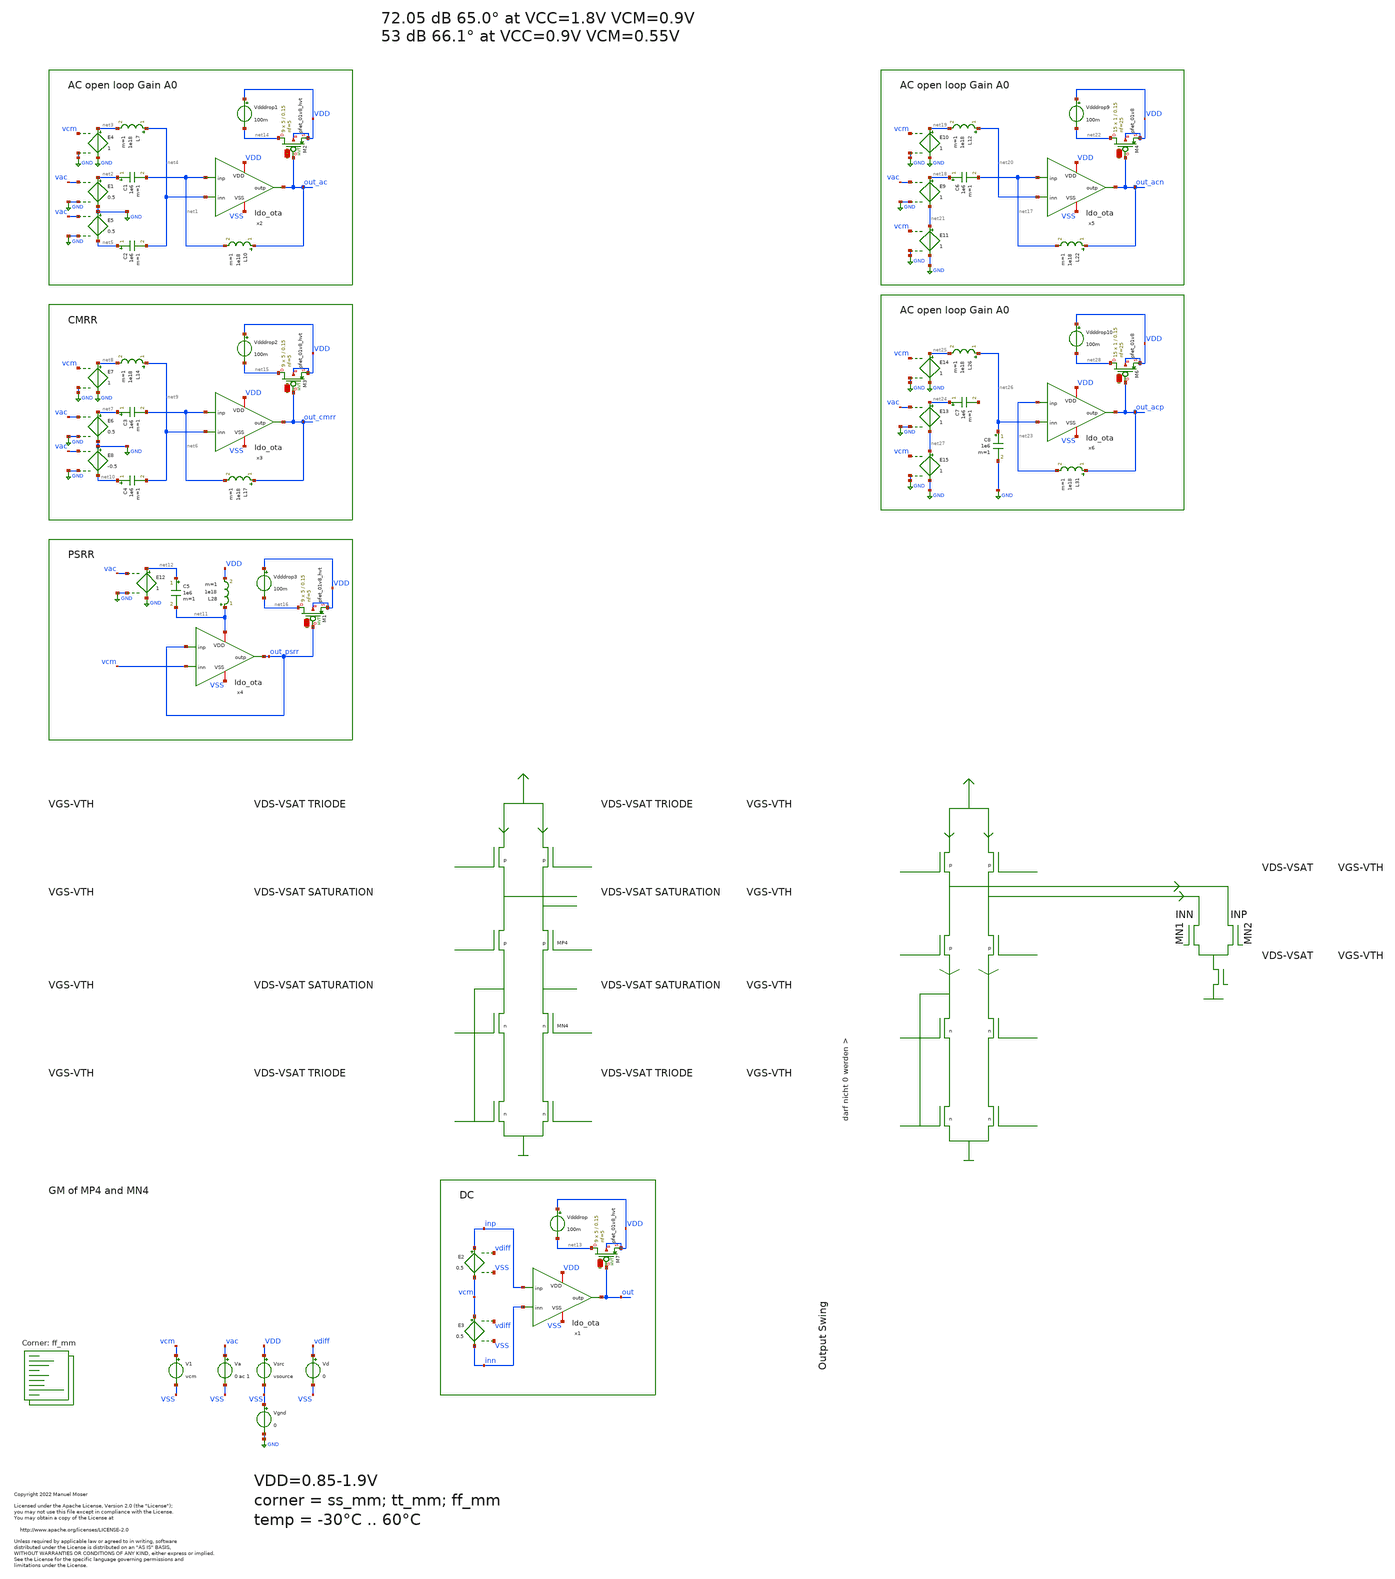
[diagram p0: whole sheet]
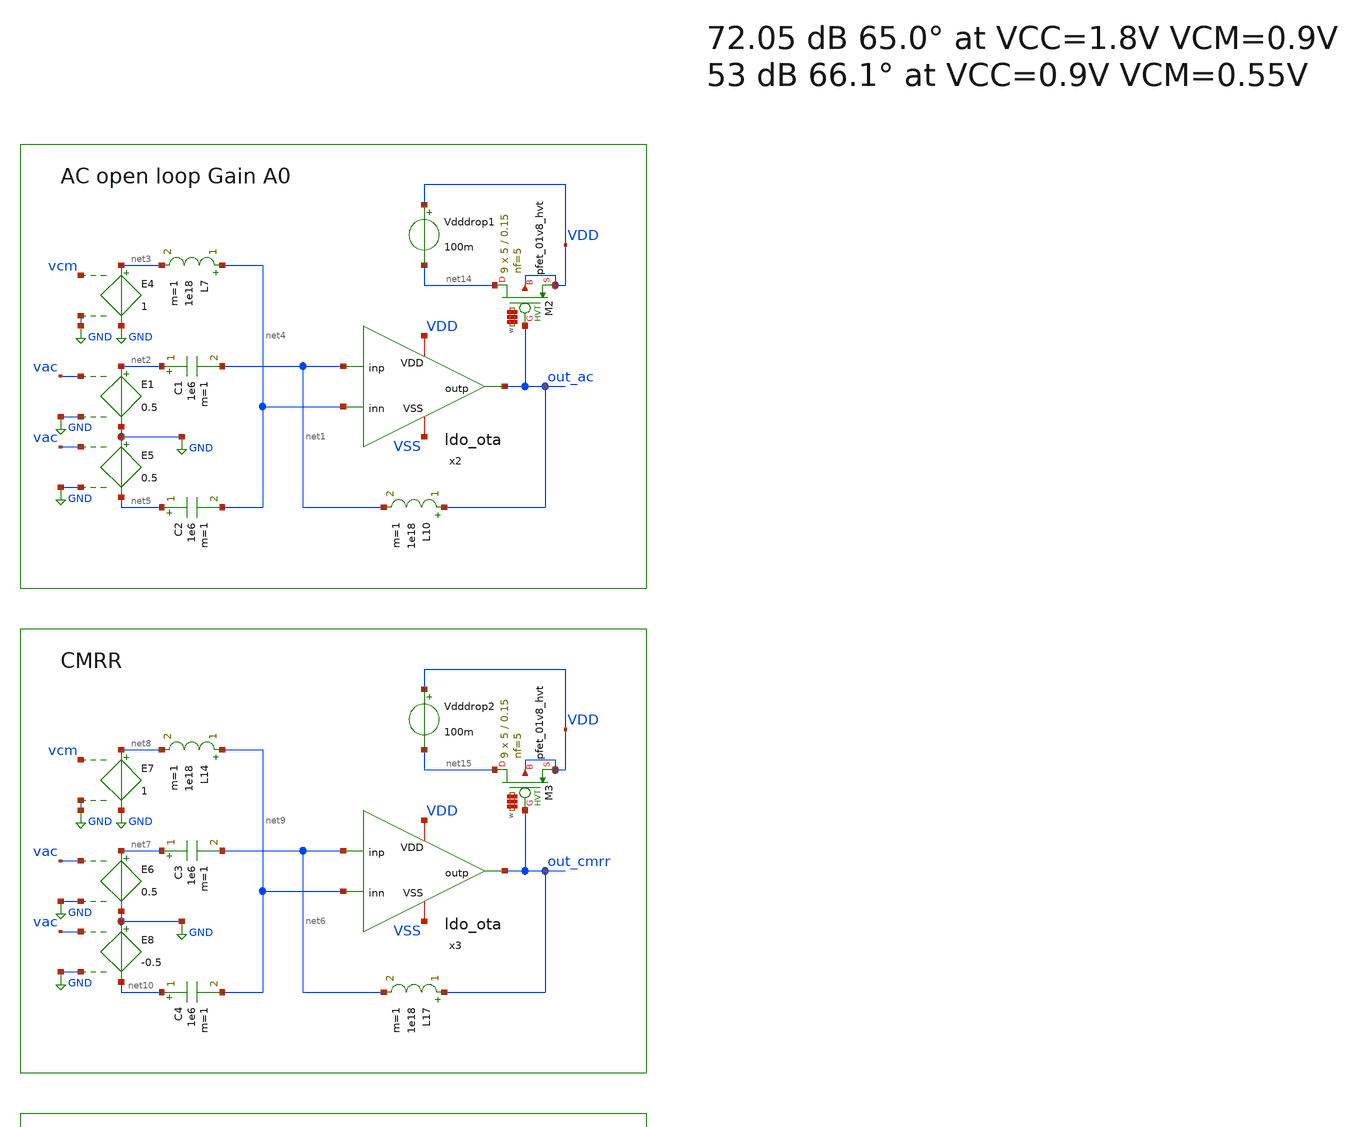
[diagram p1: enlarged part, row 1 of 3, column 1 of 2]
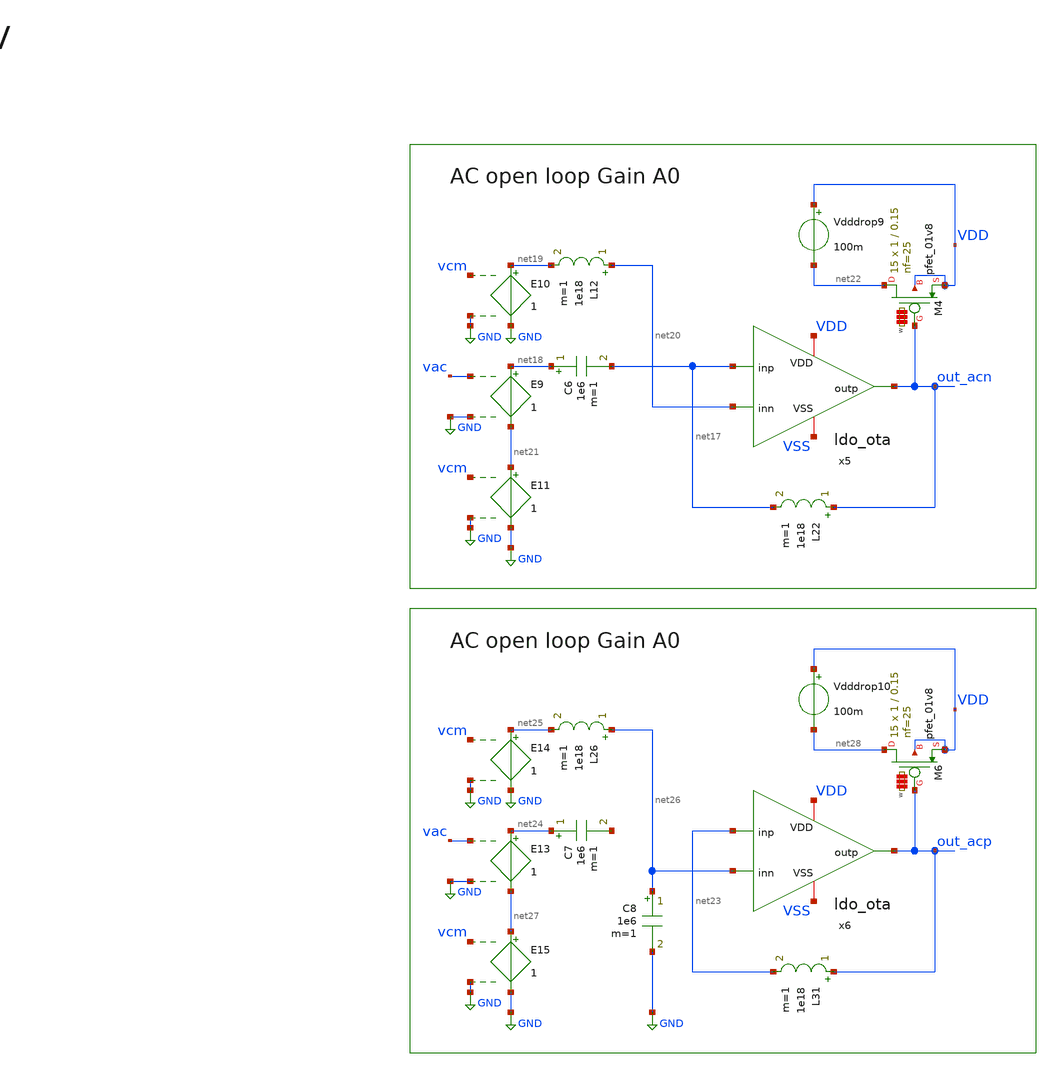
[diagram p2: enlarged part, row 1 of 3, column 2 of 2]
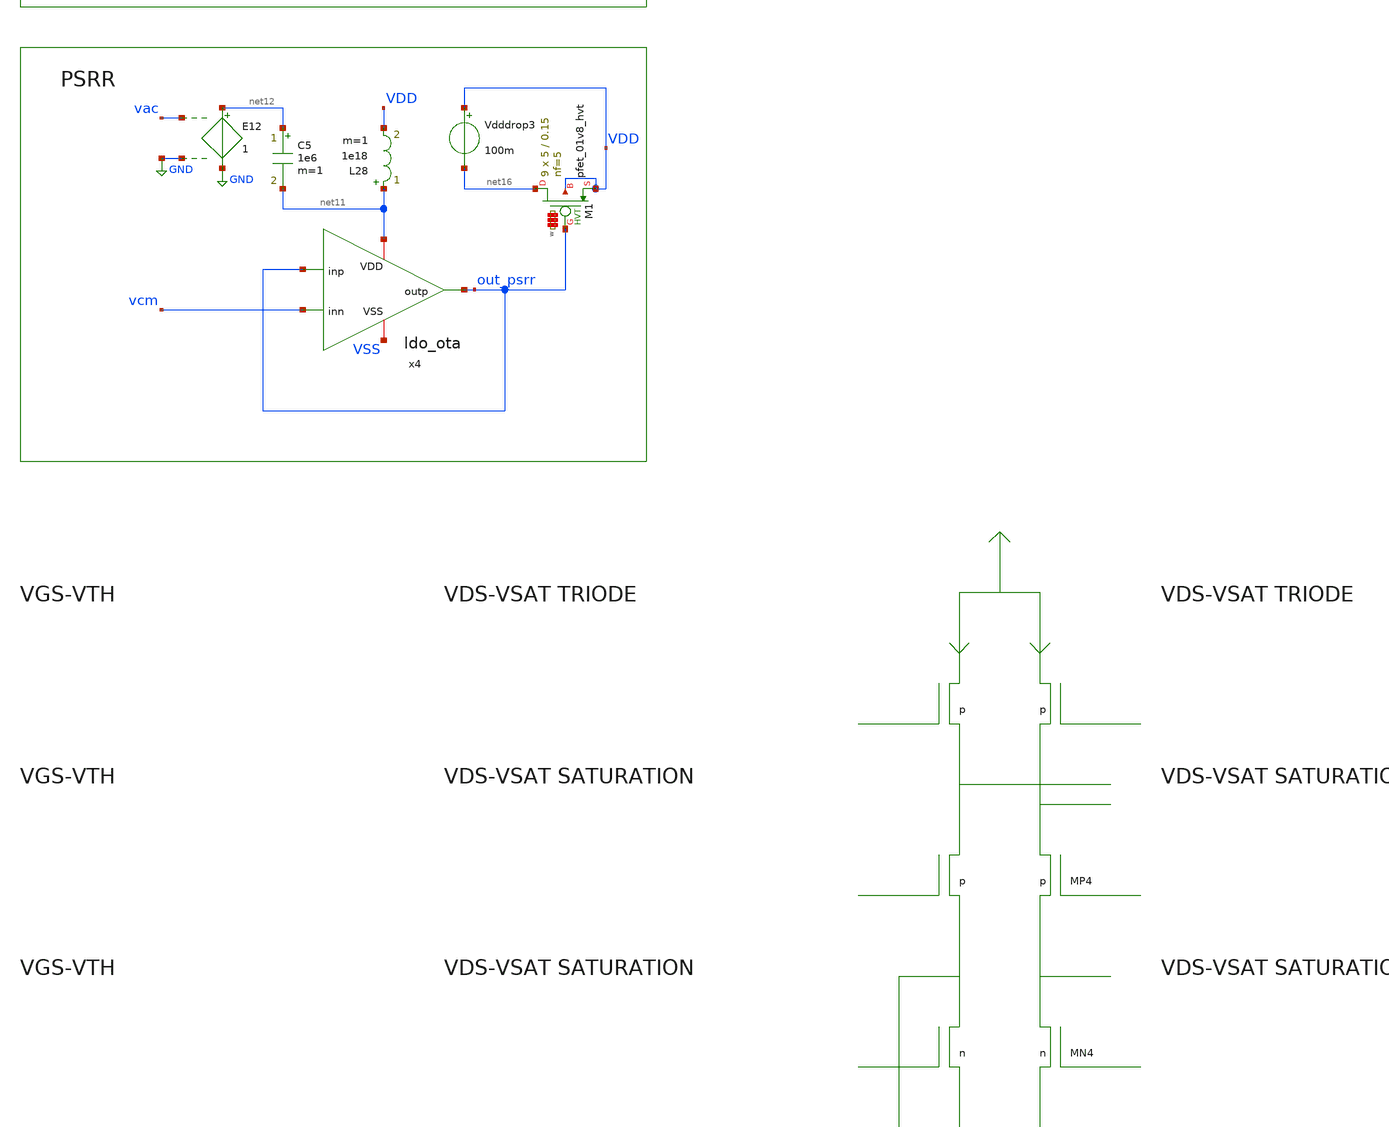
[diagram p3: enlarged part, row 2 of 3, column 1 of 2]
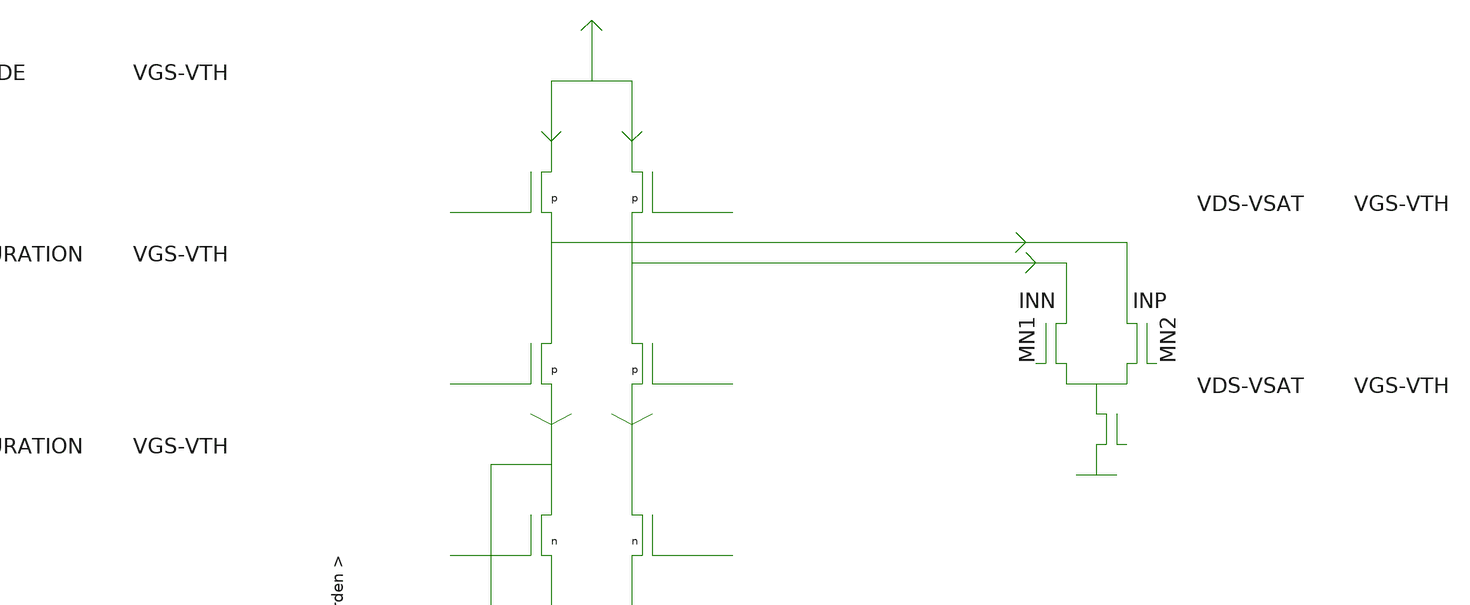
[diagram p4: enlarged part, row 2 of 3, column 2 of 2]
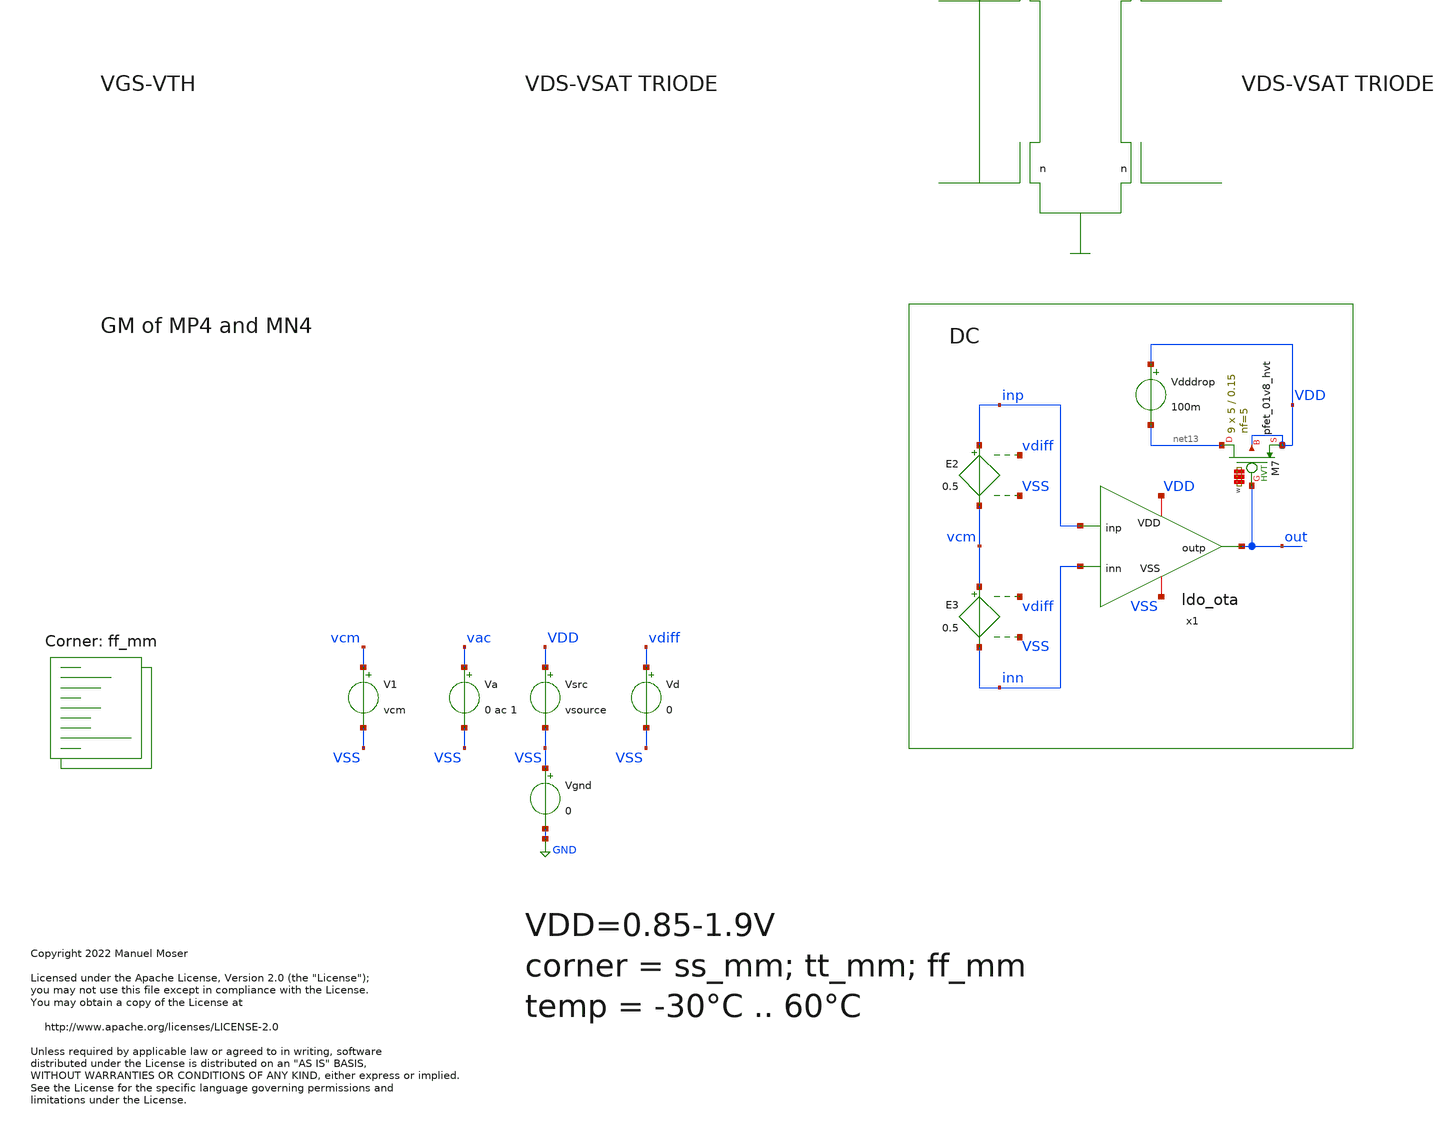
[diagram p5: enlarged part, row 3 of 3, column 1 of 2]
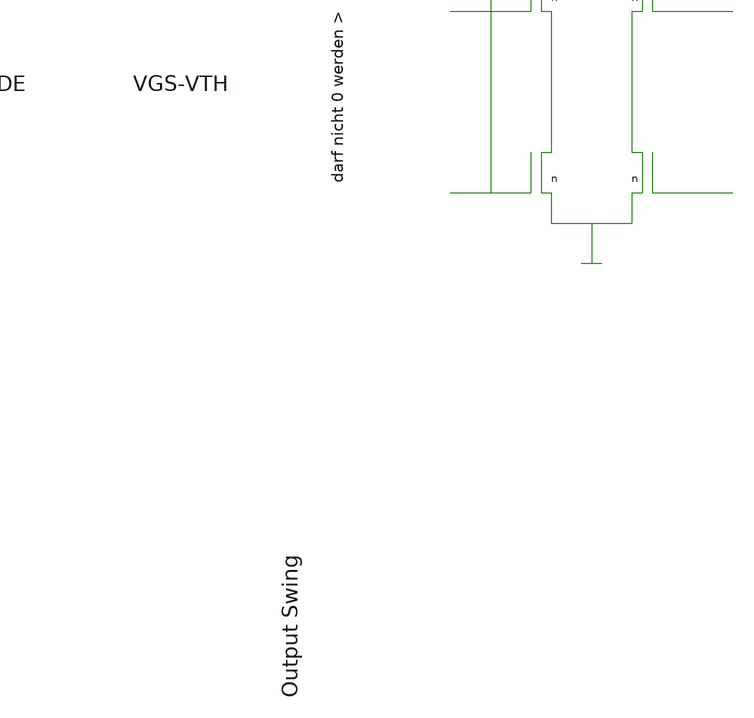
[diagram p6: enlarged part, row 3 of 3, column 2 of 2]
** sch_path: xschem/ldo_ota_tb.sch
* Copyright 2022 Manuel Moser
* Licensed under the Apache License, Version 2.0 (the "License");
**.subckt ldo_ota_tb
V1 vcm VSS vcm
Vd vdiff VSS 0
Vsrc VDD VSS vsource
E2 inp vcm vdiff VSS 0.5
E3 vcm inn vdiff VSS 0.5
Vgnd VSS GND 0
x2 VDD net1 out_ac net4 VSS ldo_ota
Va vac VSS 0 ac 1
E1 net2 GND vac GND 0.5
C1 net2 net1 1e6 m=1
L7 net4 net3 1e18 m=1
E4 net3 GND vcm GND 1
L10 out_ac net1 1e18 m=1
E5 GND net5 vac GND 0.5
C2 net5 net4 1e6 m=1
x3 VDD net6 out_cmrr net9 VSS ldo_ota
E6 net7 GND vac GND 0.5
C3 net7 net6 1e6 m=1
L14 net9 net8 1e18 m=1
E7 net8 GND vcm GND 1
L17 out_cmrr net6 1e18 m=1
E8 GND net10 vac GND -0.5
C4 net10 net9 1e6 m=1
x4 net11 out_psrr out_psrr vcm VSS ldo_ota
C5 net12 net11 1e6 m=1
L28 net11 VDD 1e18 m=1
E12 net12 GND vac GND 1
Vdddrop VDD net13 100m
Vdddrop1 VDD net14 100m
Vdddrop2 VDD net15 100m
Vdddrop3 VDD net16 100m
x1 VDD inp out inn VSS ldo_ota
x5 VDD net17 out_acn net20 VSS ldo_ota
E9 net18 net21 vac GND 1
C6 net18 net17 1e6 m=1
L12 net20 net19 1e18 m=1
E10 net19 GND vcm GND 1
L22 out_acn net17 1e18 m=1
Vdddrop9 VDD net22 100m
XM4 net22 out_acn VDD VDD sky130_fd_pr__pfet_01v8 L=0.15 W='1 * 25 ' nf=25 ad='int((nf+1)/2) * W / nf * 0.29'
+ as='int((nf+2)/2) * W / nf * 0.29' pd='2*int((nf+1)/2) * (W / nf + 0.29)' ps='2*int((nf+2)/2) * (W / nf + 0.29)'
+ nrd='0.29 / W ' nrs='0.29 / W ' sa=0 sb=0 sd=0 mult=15 m=15
E11 net21 GND vcm GND 1
E13 net24 net27 vac GND 1
C7 net24 net29 1e6 m=1
L26 net26 net25 1e18 m=1
E14 net25 GND vcm GND 1
L31 out_acp net23 1e18 m=1
Vdddrop10 VDD net28 100m
XM6 net28 out_acp VDD VDD sky130_fd_pr__pfet_01v8 L=0.15 W='1 * 25 ' nf=25 ad='int((nf+1)/2) * W / nf * 0.29'
+ as='int((nf+2)/2) * W / nf * 0.29' pd='2*int((nf+1)/2) * (W / nf + 0.29)' ps='2*int((nf+2)/2) * (W / nf + 0.29)'
+ nrd='0.29 / W ' nrs='0.29 / W ' sa=0 sb=0 sd=0 mult=15 m=15
E15 net27 GND vcm GND 1
x6 VDD net23 out_acp net26 VSS ldo_ota
C8 net26 GND 1e6 m=1
XM7 net13 out VDD VDD sky130_fd_pr__pfet_01v8_hvt L=0.15 W='5 * 5 ' nf=5 ad='int((nf+1)/2) * W / nf * 0.29'
+ as='int((nf+2)/2) * W / nf * 0.29' pd='2*int((nf+1)/2) * (W / nf + 0.29)' ps='2*int((nf+2)/2) * (W / nf + 0.29)'
+ nrd='0.29 / W ' nrs='0.29 / W ' sa=0 sb=0 sd=0 mult=9 m=9
XM1 net16 out_psrr VDD VDD sky130_fd_pr__pfet_01v8_hvt L=0.15 W='5 * 5 ' nf=5 ad='int((nf+1)/2) * W / nf * 0.29'
+ as='int((nf+2)/2) * W / nf * 0.29' pd='2*int((nf+1)/2) * (W / nf + 0.29)' ps='2*int((nf+2)/2) * (W / nf + 0.29)'
+ nrd='0.29 / W ' nrs='0.29 / W ' sa=0 sb=0 sd=0 mult=9 m=9
XM3 net15 out_cmrr VDD VDD sky130_fd_pr__pfet_01v8_hvt L=0.15 W='5 * 5 ' nf=5 ad='int((nf+1)/2) * W / nf * 0.29'
+ as='int((nf+2)/2) * W / nf * 0.29' pd='2*int((nf+1)/2) * (W / nf + 0.29)' ps='2*int((nf+2)/2) * (W / nf + 0.29)'
+ nrd='0.29 / W ' nrs='0.29 / W ' sa=0 sb=0 sd=0 mult=9 m=9
XM2 net14 out_ac VDD VDD sky130_fd_pr__pfet_01v8_hvt L=0.15 W='5 * 5 ' nf=5 ad='int((nf+1)/2) * W / nf * 0.29'
+ as='int((nf+2)/2) * W / nf * 0.29' pd='2*int((nf+1)/2) * (W / nf + 0.29)' ps='2*int((nf+2)/2) * (W / nf + 0.29)'
+ nrd='0.29 / W ' nrs='0.29 / W ' sa=0 sb=0 sd=0 mult=9 m=9
**** begin user architecture code



.temp 27
*.options savecurrents
.option gmin = 1e-16
.option RSHUNT=1E20

.param vsource = 0.9
.param vcm = {vsource/2+0.10}


.save all
 + @m.x1.x1.xmn1.msky130_fd_pr__nfet_01v8_lvt[vgs] @m.x1.x1.xmn1.msky130_fd_pr__nfet_01v8_lvt[vth]
+ @m.x1.x1.xmn1.msky130_fd_pr__nfet_01v8_lvt[vds] @m.x1.x1.xmn1.msky130_fd_pr__nfet_01v8_lvt[vdsat] @m.x1.x1.xmn1.msky130_fd_pr__nfet_01v8_lvt[id]
+ @m.x1.x1.xmn1.msky130_fd_pr__nfet_01v8_lvt[gm]
 + @m.x1.x1.xmn2.msky130_fd_pr__nfet_01v8_lvt[vgs] @m.x1.x1.xmn2.msky130_fd_pr__nfet_01v8_lvt[vth]
+ @m.x1.x1.xmn2.msky130_fd_pr__nfet_01v8_lvt[vds] @m.x1.x1.xmn2.msky130_fd_pr__nfet_01v8_lvt[vdsat] @m.x1.x1.xmn2.msky130_fd_pr__nfet_01v8_lvt[id]
+ @m.x1.x1.xmn2.msky130_fd_pr__nfet_01v8_lvt[gm]
 + @m.x1.x1.xmn3.msky130_fd_pr__nfet_01v8_lvt[vgs] @m.x1.x1.xmn3.msky130_fd_pr__nfet_01v8_lvt[vth]
+ @m.x1.x1.xmn3.msky130_fd_pr__nfet_01v8_lvt[vds] @m.x1.x1.xmn3.msky130_fd_pr__nfet_01v8_lvt[vdsat] @m.x1.x1.xmn3.msky130_fd_pr__nfet_01v8_lvt[id]
+ @m.x1.x1.xmn3.msky130_fd_pr__nfet_01v8_lvt[gm]
 + @m.x1.x1.xmn4.msky130_fd_pr__nfet_01v8_lvt[vgs] @m.x1.x1.xmn4.msky130_fd_pr__nfet_01v8_lvt[vth]
+ @m.x1.x1.xmn4.msky130_fd_pr__nfet_01v8_lvt[vds] @m.x1.x1.xmn4.msky130_fd_pr__nfet_01v8_lvt[vdsat] @m.x1.x1.xmn4.msky130_fd_pr__nfet_01v8_lvt[id]
+ @m.x1.x1.xmn4.msky130_fd_pr__nfet_01v8_lvt[gm]
 + @m.x1.x1.xmn5.msky130_fd_pr__nfet_01v8[vgs] @m.x1.x1.xmn5.msky130_fd_pr__nfet_01v8[vth]
+ @m.x1.x1.xmn5.msky130_fd_pr__nfet_01v8[vds] @m.x1.x1.xmn5.msky130_fd_pr__nfet_01v8[vdsat] @m.x1.x1.xmn5.msky130_fd_pr__nfet_01v8[id]
+ @m.x1.x1.xmn5.msky130_fd_pr__nfet_01v8[gm]
 + @m.x1.x1.xmn6.msky130_fd_pr__nfet_01v8[vgs] @m.x1.x1.xmn6.msky130_fd_pr__nfet_01v8[vth]
+ @m.x1.x1.xmn6.msky130_fd_pr__nfet_01v8[vds] @m.x1.x1.xmn6.msky130_fd_pr__nfet_01v8[vdsat] @m.x1.x1.xmn6.msky130_fd_pr__nfet_01v8[id]
+ @m.x1.x1.xmn6.msky130_fd_pr__nfet_01v8[gm]
 + @m.x1.x1.xmn7.msky130_fd_pr__nfet_01v8[vgs] @m.x1.x1.xmn7.msky130_fd_pr__nfet_01v8[vth]
+ @m.x1.x1.xmn7.msky130_fd_pr__nfet_01v8[vds] @m.x1.x1.xmn7.msky130_fd_pr__nfet_01v8[vdsat] @m.x1.x1.xmn7.msky130_fd_pr__nfet_01v8[id]
+ @m.x1.x1.xmn7.msky130_fd_pr__nfet_01v8[gm]
 + @m.x1.x1.xmp1.msky130_fd_pr__pfet_01v8_lvt[vgs] @m.x1.x1.xmp1.msky130_fd_pr__pfet_01v8_lvt[vth]
+ @m.x1.x1.xmp1.msky130_fd_pr__pfet_01v8_lvt[vds] @m.x1.x1.xmp1.msky130_fd_pr__pfet_01v8_lvt[vdsat] @m.x1.x1.xmp1.msky130_fd_pr__pfet_01v8_lvt[id]
+ @m.x1.x1.xmp1.msky130_fd_pr__pfet_01v8_lvt[gm]
 + @m.x1.x1.xmp2.msky130_fd_pr__pfet_01v8_lvt[vgs] @m.x1.x1.xmp2.msky130_fd_pr__pfet_01v8_lvt[vth]
+ @m.x1.x1.xmp2.msky130_fd_pr__pfet_01v8_lvt[vds] @m.x1.x1.xmp2.msky130_fd_pr__pfet_01v8_lvt[vdsat] @m.x1.x1.xmp2.msky130_fd_pr__pfet_01v8_lvt[id]
+ @m.x1.x1.xmp2.msky130_fd_pr__pfet_01v8_lvt[gm]
 + @m.x1.x1.xmp3.msky130_fd_pr__pfet_01v8_lvt[vgs] @m.x1.x1.xmp3.msky130_fd_pr__pfet_01v8_lvt[vth]
+ @m.x1.x1.xmp3.msky130_fd_pr__pfet_01v8_lvt[vds] @m.x1.x1.xmp3.msky130_fd_pr__pfet_01v8_lvt[vdsat] @m.x1.x1.xmp3.msky130_fd_pr__pfet_01v8_lvt[id]
+ @m.x1.x1.xmp3.msky130_fd_pr__pfet_01v8_lvt[gm]
 + @m.x1.x1.xmp4.msky130_fd_pr__pfet_01v8_lvt[vgs] @m.x1.x1.xmp4.msky130_fd_pr__pfet_01v8_lvt[vth]
+ @m.x1.x1.xmp4.msky130_fd_pr__pfet_01v8_lvt[vds] @m.x1.x1.xmp4.msky130_fd_pr__pfet_01v8_lvt[vdsat] @m.x1.x1.xmp4.msky130_fd_pr__pfet_01v8_lvt[id]
+ @m.x1.x1.xmp4.msky130_fd_pr__pfet_01v8_lvt[gm]
 + @m.x1.x1.xm9.msky130_fd_pr__nfet_01v8_lvt[vgs] @m.x1.x1.xm9.msky130_fd_pr__nfet_01v8_lvt[vth]
+ @m.x1.x1.xm9.msky130_fd_pr__nfet_01v8_lvt[vds] @m.x1.x1.xm9.msky130_fd_pr__nfet_01v8_lvt[vdsat] @m.x1.x1.xm9.msky130_fd_pr__nfet_01v8_lvt[id]
+ @m.x1.x1.xm9.msky130_fd_pr__nfet_01v8_lvt[gm]

.control
set num_threads = 12
write results.raw
*write results_ac.raw
set appendwrite

repeat 10
 reset
 dc vd -300m 300m 0.2m temp -30 60 90

write results.raw out x1.bias1 x1.bias2 x1.bias3 x1.bias4
 + @m.x1.x1.xmn1.msky130_fd_pr__nfet_01v8_lvt[vgs] @m.x1.x1.xmn1.msky130_fd_pr__nfet_01v8_lvt[vth]
+ @m.x1.x1.xmn1.msky130_fd_pr__nfet_01v8_lvt[vds] @m.x1.x1.xmn1.msky130_fd_pr__nfet_01v8_lvt[vdsat] @m.x1.x1.xmn1.msky130_fd_pr__nfet_01v8_lvt[id]
+ @m.x1.x1.xmn1.msky130_fd_pr__nfet_01v8_lvt[gm]
 + @m.x1.x1.xmn2.msky130_fd_pr__nfet_01v8_lvt[vgs] @m.x1.x1.xmn2.msky130_fd_pr__nfet_01v8_lvt[vth]
+ @m.x1.x1.xmn2.msky130_fd_pr__nfet_01v8_lvt[vds] @m.x1.x1.xmn2.msky130_fd_pr__nfet_01v8_lvt[vdsat] @m.x1.x1.xmn2.msky130_fd_pr__nfet_01v8_lvt[id]
+ @m.x1.x1.xmn2.msky130_fd_pr__nfet_01v8_lvt[gm]
 + @m.x1.x1.xmn3.msky130_fd_pr__nfet_01v8_lvt[vgs] @m.x1.x1.xmn3.msky130_fd_pr__nfet_01v8_lvt[vth]
+ @m.x1.x1.xmn3.msky130_fd_pr__nfet_01v8_lvt[vds] @m.x1.x1.xmn3.msky130_fd_pr__nfet_01v8_lvt[vdsat] @m.x1.x1.xmn3.msky130_fd_pr__nfet_01v8_lvt[id]
+ @m.x1.x1.xmn3.msky130_fd_pr__nfet_01v8_lvt[gm]
 + @m.x1.x1.xmn4.msky130_fd_pr__nfet_01v8_lvt[vgs] @m.x1.x1.xmn4.msky130_fd_pr__nfet_01v8_lvt[vth]
+ @m.x1.x1.xmn4.msky130_fd_pr__nfet_01v8_lvt[vds] @m.x1.x1.xmn4.msky130_fd_pr__nfet_01v8_lvt[vdsat] @m.x1.x1.xmn4.msky130_fd_pr__nfet_01v8_lvt[id]
+ @m.x1.x1.xmn4.msky130_fd_pr__nfet_01v8_lvt[gm]
 + @m.x1.x1.xmn5.msky130_fd_pr__nfet_01v8[vgs] @m.x1.x1.xmn5.msky130_fd_pr__nfet_01v8[vth]
+ @m.x1.x1.xmn5.msky130_fd_pr__nfet_01v8[vds] @m.x1.x1.xmn5.msky130_fd_pr__nfet_01v8[vdsat] @m.x1.x1.xmn5.msky130_fd_pr__nfet_01v8[id]
+ @m.x1.x1.xmn5.msky130_fd_pr__nfet_01v8[gm]
 + @m.x1.x1.xmn6.msky130_fd_pr__nfet_01v8[vgs] @m.x1.x1.xmn6.msky130_fd_pr__nfet_01v8[vth]
+ @m.x1.x1.xmn6.msky130_fd_pr__nfet_01v8[vds] @m.x1.x1.xmn6.msky130_fd_pr__nfet_01v8[vdsat] @m.x1.x1.xmn6.msky130_fd_pr__nfet_01v8[id]
+ @m.x1.x1.xmn6.msky130_fd_pr__nfet_01v8[gm]
 + @m.x1.x1.xmn7.msky130_fd_pr__nfet_01v8[vgs] @m.x1.x1.xmn7.msky130_fd_pr__nfet_01v8[vth]
+ @m.x1.x1.xmn7.msky130_fd_pr__nfet_01v8[vds] @m.x1.x1.xmn7.msky130_fd_pr__nfet_01v8[vdsat] @m.x1.x1.xmn7.msky130_fd_pr__nfet_01v8[id]
+ @m.x1.x1.xmn7.msky130_fd_pr__nfet_01v8[gm]
 + @m.x1.x1.xmp1.msky130_fd_pr__pfet_01v8_lvt[vgs] @m.x1.x1.xmp1.msky130_fd_pr__pfet_01v8_lvt[vth]
+ @m.x1.x1.xmp1.msky130_fd_pr__pfet_01v8_lvt[vds] @m.x1.x1.xmp1.msky130_fd_pr__pfet_01v8_lvt[vdsat] @m.x1.x1.xmp1.msky130_fd_pr__pfet_01v8_lvt[id]
+ @m.x1.x1.xmp1.msky130_fd_pr__pfet_01v8_lvt[gm]
 + @m.x1.x1.xmp2.msky130_fd_pr__pfet_01v8_lvt[vgs] @m.x1.x1.xmp2.msky130_fd_pr__pfet_01v8_lvt[vth]
+ @m.x1.x1.xmp2.msky130_fd_pr__pfet_01v8_lvt[vds] @m.x1.x1.xmp2.msky130_fd_pr__pfet_01v8_lvt[vdsat] @m.x1.x1.xmp2.msky130_fd_pr__pfet_01v8_lvt[id]
+ @m.x1.x1.xmp2.msky130_fd_pr__pfet_01v8_lvt[gm]
 + @m.x1.x1.xmp3.msky130_fd_pr__pfet_01v8_lvt[vgs] @m.x1.x1.xmp3.msky130_fd_pr__pfet_01v8_lvt[vth]
+ @m.x1.x1.xmp3.msky130_fd_pr__pfet_01v8_lvt[vds] @m.x1.x1.xmp3.msky130_fd_pr__pfet_01v8_lvt[vdsat] @m.x1.x1.xmp3.msky130_fd_pr__pfet_01v8_lvt[id]
+ @m.x1.x1.xmp3.msky130_fd_pr__pfet_01v8_lvt[gm]
 + @m.x1.x1.xmp4.msky130_fd_pr__pfet_01v8_lvt[vgs] @m.x1.x1.xmp4.msky130_fd_pr__pfet_01v8_lvt[vth]
+ @m.x1.x1.xmp4.msky130_fd_pr__pfet_01v8_lvt[vds] @m.x1.x1.xmp4.msky130_fd_pr__pfet_01v8_lvt[vdsat] @m.x1.x1.xmp4.msky130_fd_pr__pfet_01v8_lvt[id]
+ @m.x1.x1.xmp4.msky130_fd_pr__pfet_01v8_lvt[gm]
 + @m.x1.x1.xm9.msky130_fd_pr__nfet_01v8_lvt[vgs] @m.x1.x1.xm9.msky130_fd_pr__nfet_01v8_lvt[vth]
+ @m.x1.x1.xm9.msky130_fd_pr__nfet_01v8_lvt[vds] @m.x1.x1.xm9.msky130_fd_pr__nfet_01v8_lvt[vdsat] @m.x1.x1.xm9.msky130_fd_pr__nfet_01v8_lvt[id]
+ @m.x1.x1.xm9.msky130_fd_pr__nfet_01v8_lvt[gm]

 ac dec 10 1 10meg
 write results.raw out_ac out_cmrr out_psrr

end

.endc



.lib $::SKYWATER_MODELS/sky130.lib.spice ff_mm
**** end user architecture code
**.ends
.GLOBAL GND
.end
